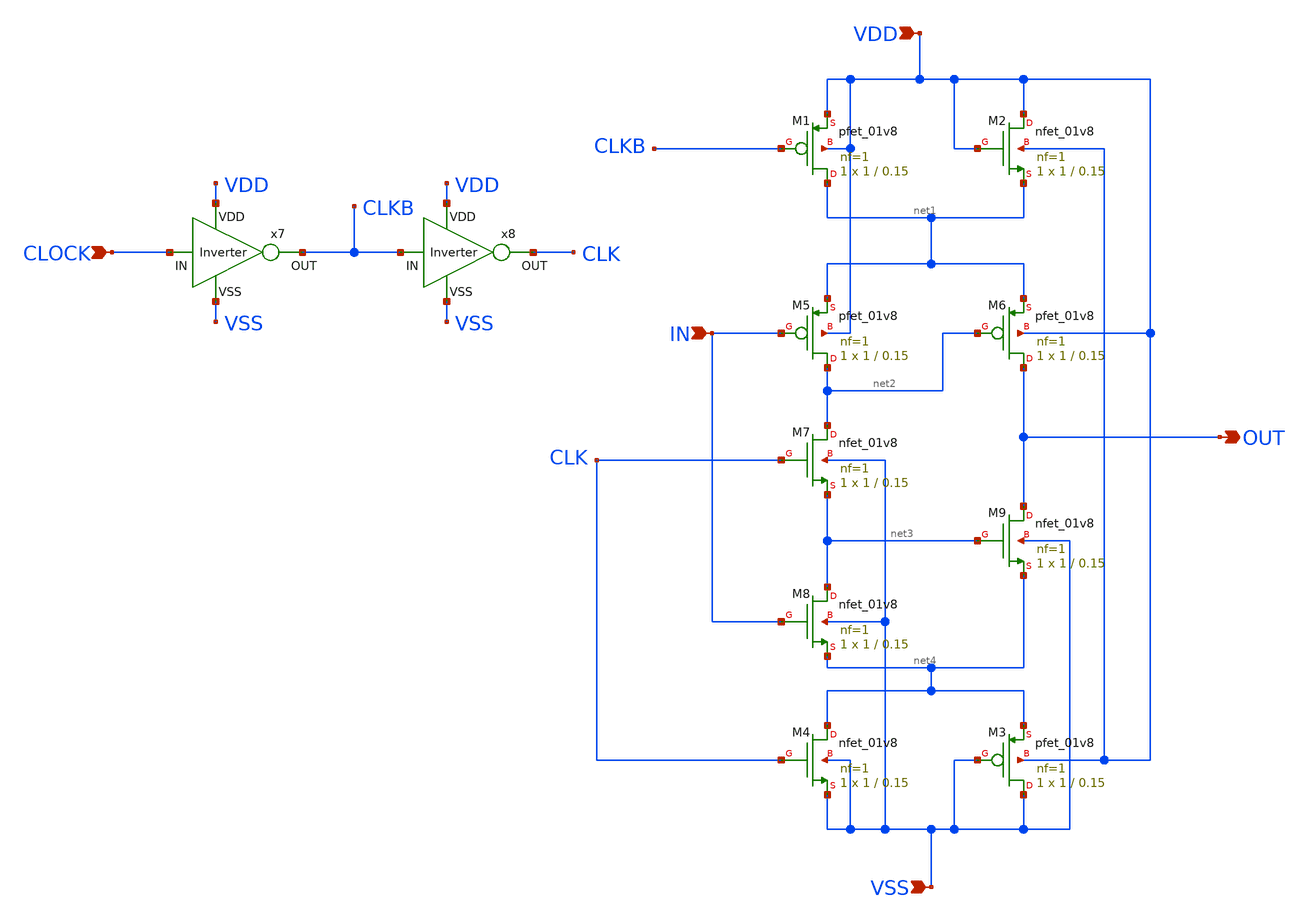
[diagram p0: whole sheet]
** sch_path: FFD_SVL.sch
**.subckt FFD_SVL VDD VSS OUT IN CLOCK
*.ipin VDD
*.ipin VSS
*.opin OUT
*.ipin IN
*.ipin CLOCK
XM1 net1 CLKB VDD VDD sky130_fd_pr__pfet_01v8 L=0.15 W=1 nf=1 ad='int((nf+1)/2) * W/nf * 0.29' as='int((nf+2)/2) * W/nf * 0.29'
+ pd='2*int((nf+1)/2) * (W/nf + 0.29)' ps='2*int((nf+2)/2) * (W/nf + 0.29)' nrd='0.29 / W' nrs='0.29 / W'
+ sa=0 sb=0 sd=0 mult=1 m=1
XM2 VDD VDD net1 VDD sky130_fd_pr__nfet_01v8 L=0.15 W=1 nf=1 ad='int((nf+1)/2) * W/nf * 0.29' as='int((nf+2)/2) * W/nf * 0.29'
+ pd='2*int((nf+1)/2) * (W/nf + 0.29)' ps='2*int((nf+2)/2) * (W/nf + 0.29)' nrd='0.29 / W' nrs='0.29 / W'
+ sa=0 sb=0 sd=0 mult=1 m=1
XM3 VSS VSS net4 VDD sky130_fd_pr__pfet_01v8 L=0.15 W=1 nf=1 ad='int((nf+1)/2) * W/nf * 0.29' as='int((nf+2)/2) * W/nf * 0.29'
+ pd='2*int((nf+1)/2) * (W/nf + 0.29)' ps='2*int((nf+2)/2) * (W/nf + 0.29)' nrd='0.29 / W' nrs='0.29 / W'
+ sa=0 sb=0 sd=0 mult=1 m=1
XM4 net4 CLK VSS VSS sky130_fd_pr__nfet_01v8 L=0.15 W=1 nf=1 ad='int((nf+1)/2) * W/nf * 0.29' as='int((nf+2)/2) * W/nf * 0.29'
+ pd='2*int((nf+1)/2) * (W/nf + 0.29)' ps='2*int((nf+2)/2) * (W/nf + 0.29)' nrd='0.29 / W' nrs='0.29 / W'
+ sa=0 sb=0 sd=0 mult=1 m=1
XM5 net2 IN net1 VDD sky130_fd_pr__pfet_01v8 L=0.15 W=1 nf=1 ad='int((nf+1)/2) * W/nf * 0.29' as='int((nf+2)/2) * W/nf * 0.29'
+ pd='2*int((nf+1)/2) * (W/nf + 0.29)' ps='2*int((nf+2)/2) * (W/nf + 0.29)' nrd='0.29 / W' nrs='0.29 / W'
+ sa=0 sb=0 sd=0 mult=1 m=1
XM6 OUT net2 net1 VDD sky130_fd_pr__pfet_01v8 L=0.15 W=1 nf=1 ad='int((nf+1)/2) * W/nf * 0.29' as='int((nf+2)/2) * W/nf * 0.29'
+ pd='2*int((nf+1)/2) * (W/nf + 0.29)' ps='2*int((nf+2)/2) * (W/nf + 0.29)' nrd='0.29 / W' nrs='0.29 / W'
+ sa=0 sb=0 sd=0 mult=1 m=1
XM7 net2 CLK net3 VSS sky130_fd_pr__nfet_01v8 L=0.15 W=1 nf=1 ad='int((nf+1)/2) * W/nf * 0.29' as='int((nf+2)/2) * W/nf * 0.29'
+ pd='2*int((nf+1)/2) * (W/nf + 0.29)' ps='2*int((nf+2)/2) * (W/nf + 0.29)' nrd='0.29 / W' nrs='0.29 / W'
+ sa=0 sb=0 sd=0 mult=1 m=1
XM8 net3 IN net4 VSS sky130_fd_pr__nfet_01v8 L=0.15 W=1 nf=1 ad='int((nf+1)/2) * W/nf * 0.29' as='int((nf+2)/2) * W/nf * 0.29'
+ pd='2*int((nf+1)/2) * (W/nf + 0.29)' ps='2*int((nf+2)/2) * (W/nf + 0.29)' nrd='0.29 / W' nrs='0.29 / W'
+ sa=0 sb=0 sd=0 mult=1 m=1
XM9 OUT net3 net4 VSS sky130_fd_pr__nfet_01v8 L=0.15 W=1 nf=1 ad='int((nf+1)/2) * W/nf * 0.29' as='int((nf+2)/2) * W/nf * 0.29'
+ pd='2*int((nf+1)/2) * (W/nf + 0.29)' ps='2*int((nf+2)/2) * (W/nf + 0.29)' nrd='0.29 / W' nrs='0.29 / W'
+ sa=0 sb=0 sd=0 mult=1 m=1
x7 VDD CLOCK CLKB VSS Inverter
x8 VDD CLKB CLK VSS Inverter
**.ends

* expanding   symbol:  project/Inverter.sym # of pins=4
** sym_path: Inverter.sym
** sch_path: Inverter.sch
.subckt Inverter VDD IN OUT VSS
*.ipin IN
*.ipin VSS
*.ipin VDD
*.opin OUT
XM1 OUT IN VSS VSS sky130_fd_pr__nfet_01v8 L=0.3 W=1 nf=1 ad='int((nf+1)/2) * W/nf * 0.29' as='int((nf+2)/2) * W/nf * 0.29'
+ pd='2*int((nf+1)/2) * (W/nf + 0.29)' ps='2*int((nf+2)/2) * (W/nf + 0.29)' nrd='0.29 / W' nrs='0.29 / W'
+ sa=0 sb=0 sd=0 mult=1 m=1
XM2 OUT IN VDD VDD sky130_fd_pr__pfet_01v8 L=0.3 W=2 nf=1 ad='int((nf+1)/2) * W/nf * 0.29' as='int((nf+2)/2) * W/nf * 0.29'
+ pd='2*int((nf+1)/2) * (W/nf + 0.29)' ps='2*int((nf+2)/2) * (W/nf + 0.29)' nrd='0.29 / W' nrs='0.29 / W'
+ sa=0 sb=0 sd=0 mult=1 m=1
.ends

.end
